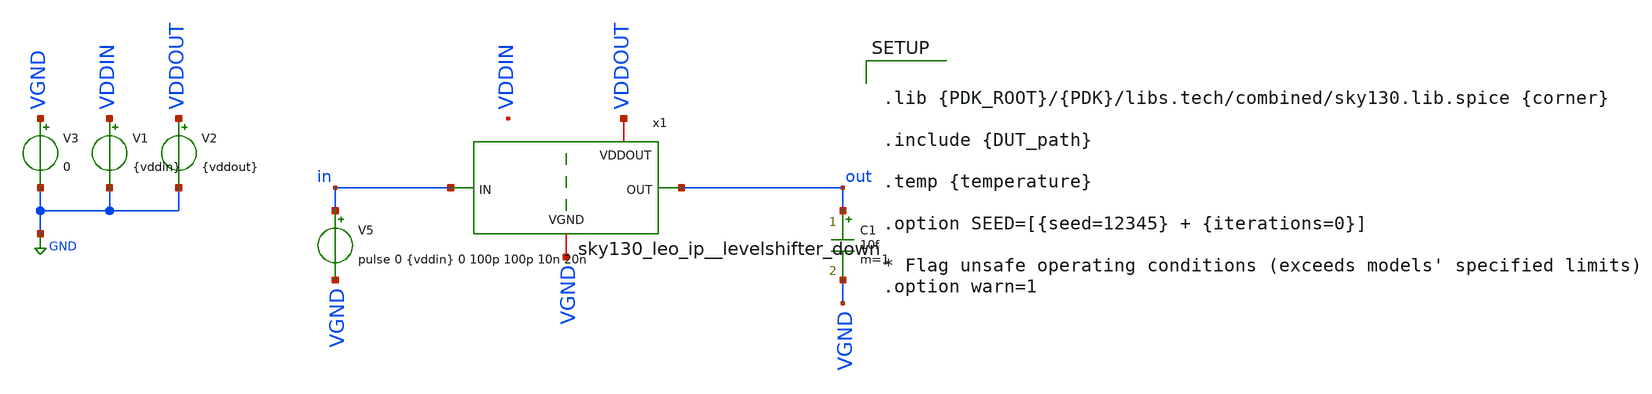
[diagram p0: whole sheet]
** sch_path: cace/templates/rise_fall_down.sch
**.subckt rise_fall_down
x1 VDDOUT out in VGND sky130_leo_ip__levelshifter_down
V1 VDDIN GND {vddin}
V2 VDDOUT GND {vddout}
V3 VGND GND 0
C1 out VGND 10f m=1
V5 in VGND pulse 0 {vddin} 0 100p 100p 10n 20n
**** begin user architecture code




.control
    * operating point
    *op
    *write tb.raw
    *set appendwrite

    * transient simulation
    options method=gear
    tran 1p 40n
    *save all
    *write tb.raw

    * measure parameters

    * get the peak-to-peak voltage
    meas TRAN range PP v(out)
    let ten=0.1*range
    let ninety=0.9*range

    print range ten ninety

    # rise and fall time
    meas TRAN rise_time TRIG v(out) VAL=ten    TD=0ns  RISE=1   TARG v(out) VAL=ninety TD=0ns
+  RISE=1
    meas TRAN fall_time TRIG v(out) VAL=ninety TD=5ns  FALL=1   TARG v(out) VAL=TEN    TD=5ns
+  FALL=1

    print rise_time fall_time

    echo $&rise_time $&fall_time > {simpath}/{filename}_{N}.data

.endc





.lib {PDK_ROOT}/{PDK}/libs.tech/combined/sky130.lib.spice {corner}

.include {DUT_path}

.temp {temperature}

.option SEED=[{seed=12345} + {iterations=0}]

* Flag unsafe operating conditions (exceeds models' specified limits)
.option warn=1


**** end user architecture code
**.ends

* expanding   symbol:  sky130_leo_ip__levelshifter_down.sym # of pins=4
** sym_path: xschem/sky130_leo_ip__levelshifter_down.sym
** sch_path: xschem/sky130_leo_ip__levelshifter_down.sch
.subckt sky130_leo_ip__levelshifter_down VDDOUT OUT IN VGND
*.ipin IN
*.iopin VGND
*.ipin OUT
*.iopin VDDOUT
XM3 OUT n VGND VGND sky130_fd_pr__nfet_01v8 L=0.15 W=0.42 nf=1 ad='int((nf+1)/2) * W/nf * 0.29' as='int((nf+2)/2)
+ * W/nf * 0.29' pd='2*int((nf+1)/2) * (W/nf + 0.29)' ps='2*int((nf+2)/2) * (W/nf + 0.29)' nrd='0.29 /
+ W' nrs='0.29 / W' sa=0 sb=0 sd=0 mult=1 m=1
XM4 OUT n VDDOUT VDDOUT sky130_fd_pr__pfet_01v8 L=0.15 W=1 nf=1 ad='int((nf+1)/2) * W/nf * 0.29' as='int((nf+2)/2)
+ * W/nf * 0.29' pd='2*int((nf+1)/2) * (W/nf + 0.29)' ps='2*int((nf+2)/2) * (W/nf + 0.29)' nrd='0.29 /
+ W' nrs='0.29 / W' sa=0 sb=0 sd=0 mult=1 m=1
XM5 n IN VDDOUT VDDOUT sky130_fd_pr__pfet_g5v0d10v5 L=0.5 W=0.42 nf=1 ad='int((nf+1)/2) * W/nf * 0.29' as='int((nf+2)/2)
+ * W/nf * 0.29' pd='2*int((nf+1)/2) * (W/nf + 0.29)' ps='2*int((nf+2)/2) * (W/nf + 0.29)' nrd='0.29 /
+ W' nrs='0.29 / W' sa=0 sb=0 sd=0 mult=1 m=1
XM6 n IN VGND VGND sky130_fd_pr__nfet_g5v0d10v5 L=0.5 W=1 nf=1 ad='int((nf+1)/2) * W/nf * 0.29' as='int((nf+2)/2)
+ * W/nf * 0.29' pd='2*int((nf+1)/2) * (W/nf + 0.29)' ps='2*int((nf+2)/2) * (W/nf + 0.29)' nrd='0.29 /
+ W' nrs='0.29 / W' sa=0 sb=0 sd=0 mult=1 m=1
.ends

.GLOBAL GND
.end
